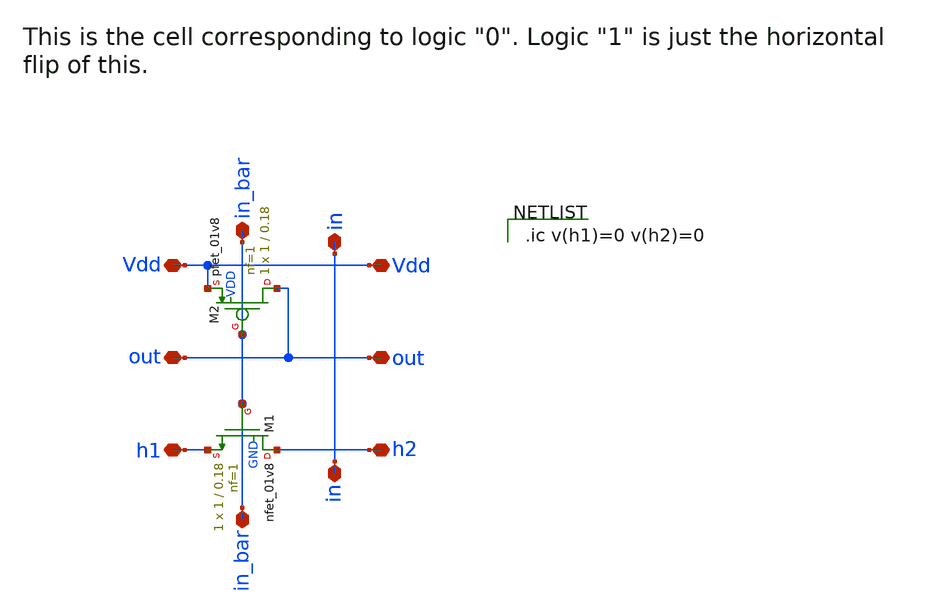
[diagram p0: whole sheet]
** sch_path: xschem/decoder/decoder_cell_0.sch
**.subckt decoder_cell_0 out h2 Vdd h1 out Vdd in in in_bar in_bar out h2 Vdd h1 out Vdd in in
*.iopin out
*.iopin h2
*.iopin Vdd
*.iopin h1
*.iopin out
*.iopin Vdd
*.iopin in
*.iopin in
*.iopin in_bar
*.iopin in_bar
*.iopin out
*.iopin h2
*.iopin Vdd
*.iopin h1
*.iopin out
*.iopin Vdd
*.iopin in
*.iopin in
XM1 h2 in_bar h1 GND sky130_fd_pr__nfet_01v8 L=0.18 W=1 nf=1 ad='int((nf+1)/2) * W/nf * 0.29' as='int((nf+2)/2) * W/nf * 0.29'
+ pd='2*int((nf+1)/2) * (W/nf + 0.29)' ps='2*int((nf+2)/2) * (W/nf + 0.29)' nrd='0.29 / W' nrs='0.29 / W'
+ sa=0 sb=0 sd=0 mult=1 m=1
XM2 out in_bar Vdd VDD sky130_fd_pr__pfet_01v8 L=0.18 W=1 nf=1 ad='int((nf+1)/2) * W/nf * 0.29' as='int((nf+2)/2) * W/nf * 0.29'
+ pd='2*int((nf+1)/2) * (W/nf + 0.29)' ps='2*int((nf+2)/2) * (W/nf + 0.29)' nrd='0.29 / W' nrs='0.29 / W'
+ sa=0 sb=0 sd=0 mult=1 m=1
**** begin user architecture code

.ic v(h1)=0 v(h2)=0

**** end user architecture code
**.ends
.end
